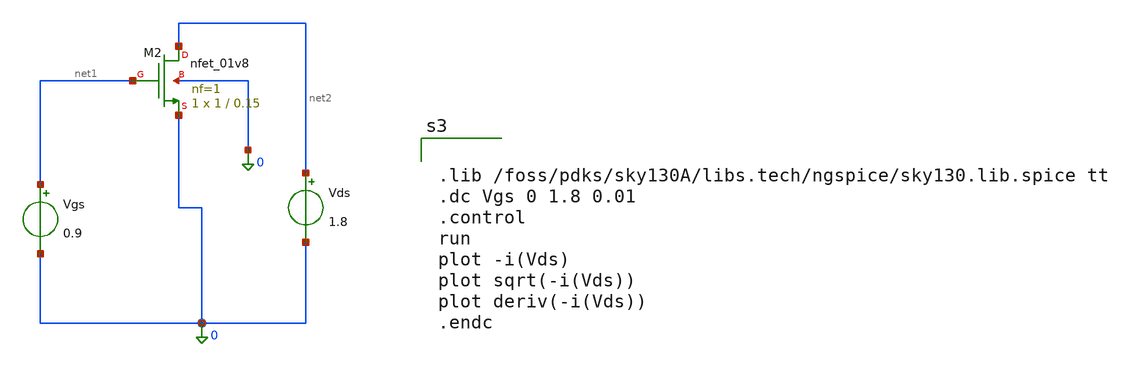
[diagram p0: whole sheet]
** sch_path: week1_mos_characterization/nmos_idvgs.sch
**.subckt nmos_idvgs
XM2 net2 net1 0 0 sky130_fd_pr__nfet_01v8 L=0.15 W=1 nf=1 ad='int((1 + 1)/2) * 1 / 1 * 0.29' as='int((1 + 2)/2) * 1 / 1 * 0.29'
+ pd='2*int((1 + 1)/2) * (1 / 1 + 0.29)' ps='2*int((1 + 2)/2) * (1 / 1 + 0.29)' nrd='0.29 / 1 ' nrs='0.29 / 1 '
+ sa=0 sb=0 sd=0 mult=1 m=1
Vgs net1 0 0.9
Vds net2 0 1.8
**** begin user architecture code


.lib /foss/pdks/sky130A/libs.tech/ngspice/sky130.lib.spice tt
.dc Vgs 0 1.8 0.01
.control
run
plot -i(Vds)
plot sqrt(-i(Vds))
plot deriv(-i(Vds))
.endc


**** end user architecture code
**.ends
.end
